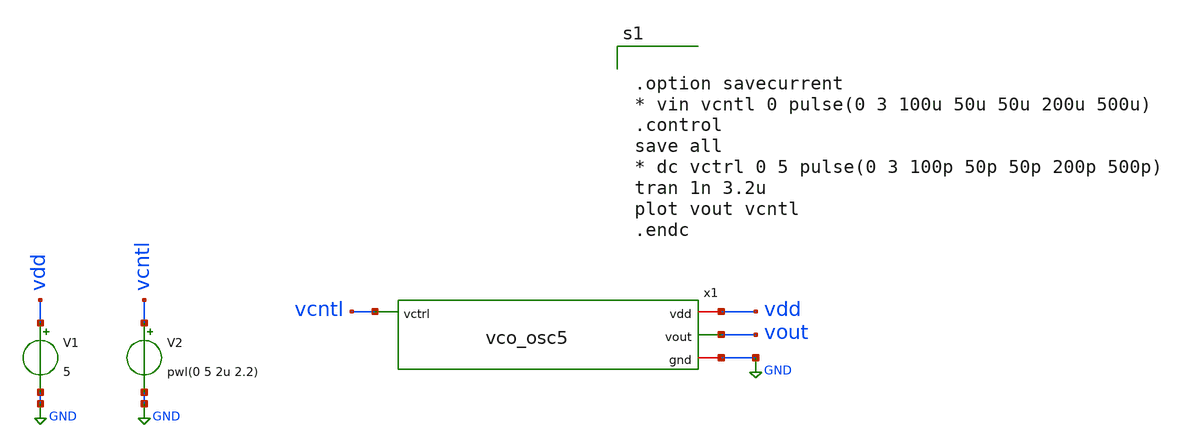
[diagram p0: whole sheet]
** sch_path: member_project/Sinby/tb_vco_osc5.sch
**.subckt tb_vco_osc5
x1 vdd vout vcntl GND vco_osc5
V1 vdd GND 5
V2 vcntl GND pwl(0 5 2u 2.2)
**** begin user architecture code
 .include $::LIB/mos.lib
.include $::LIB/passive.lib
.include $::LIB/diode.lib


.option savecurrent
* vin vcntl 0 pulse(0 3 100u 50u 50u 200u 500u)
.control
save all
* dc vctrl 0 5 pulse(0 3 100p 50p 50p 200p 500p)
tran 1n 3.2u
plot vout vcntl
.endc


**** end user architecture code
**.ends

* expanding   symbol:  vco_osc5.sym # of pins=4
** sym_path: member_project/Sinby/vco_osc5.sym
** sch_path: member_project/Sinby/vco_osc5.sch
.subckt vco_osc5 vdd vout vctrl gnd
*.iopin vdd
*.iopin gnd
*.opin vout
*.ipin vctrl
M1 vout net1 gnd gnd nchor1ex L=1u W=8u m=1
M4 vout net1 vdd vdd pchor1ex L=1u W=30u m=1
M2 net1 net2 gnd gnd nchor1ex L=1u W=2u m=1
M3 net1 net2 vdd vdd pchor1ex L=1u W=6u m=1
M5 net2 net3 net4 gnd nchor1ex L=1u W=2u m=1
M6 net2 net3 net5 vdd pchor1ex L=1u W=6u m=1
M7 net4 vctrl gnd gnd nchor1ex L=1u W=2u m=1
M8 net5 net9 vdd vdd pchor1ex L=1u W=6u m=1
M9 net3 net6 net7 gnd nchor1ex L=1u W=2u m=1
M10 net3 net6 net8 vdd pchor1ex L=1u W=6u m=1
M11 net7 vctrl gnd gnd nchor1ex L=1u W=2u m=1
M12 net8 net9 vdd vdd pchor1ex L=1u W=6u m=1
M13 net6 net10 net11 gnd nchor1ex L=1u W=2u m=1
M14 net6 net10 net12 vdd pchor1ex L=1u W=6u m=1
M15 net11 vctrl gnd gnd nchor1ex L=1u W=2u m=1
M16 net12 net9 vdd vdd pchor1ex L=1u W=6u m=1
M17 net10 net13 net14 gnd nchor1ex L=1u W=2u m=1
M18 net10 net13 net15 vdd pchor1ex L=1u W=6u m=1
M19 net14 vctrl gnd gnd nchor1ex L=1u W=2u m=1
M20 net15 net9 vdd vdd pchor1ex L=1u W=6u m=1
M21 net13 net2 net16 gnd nchor1ex L=1u W=2u m=1
M22 net13 net2 net17 vdd pchor1ex L=1u W=6u m=1
M23 net16 vctrl gnd gnd nchor1ex L=1u W=2u m=1
M24 net17 net9 vdd vdd pchor1ex L=1u W=6u m=1
M25 net9 net9 vdd vdd pchor1ex L=1u W=6u m=1
M26 net9 net9 net18 gnd nchor1ex L=1u W=2u m=1
M27 net18 vctrl gnd gnd nchor1ex L=1u W=2u m=1
.ends

.GLOBAL GND
.end
